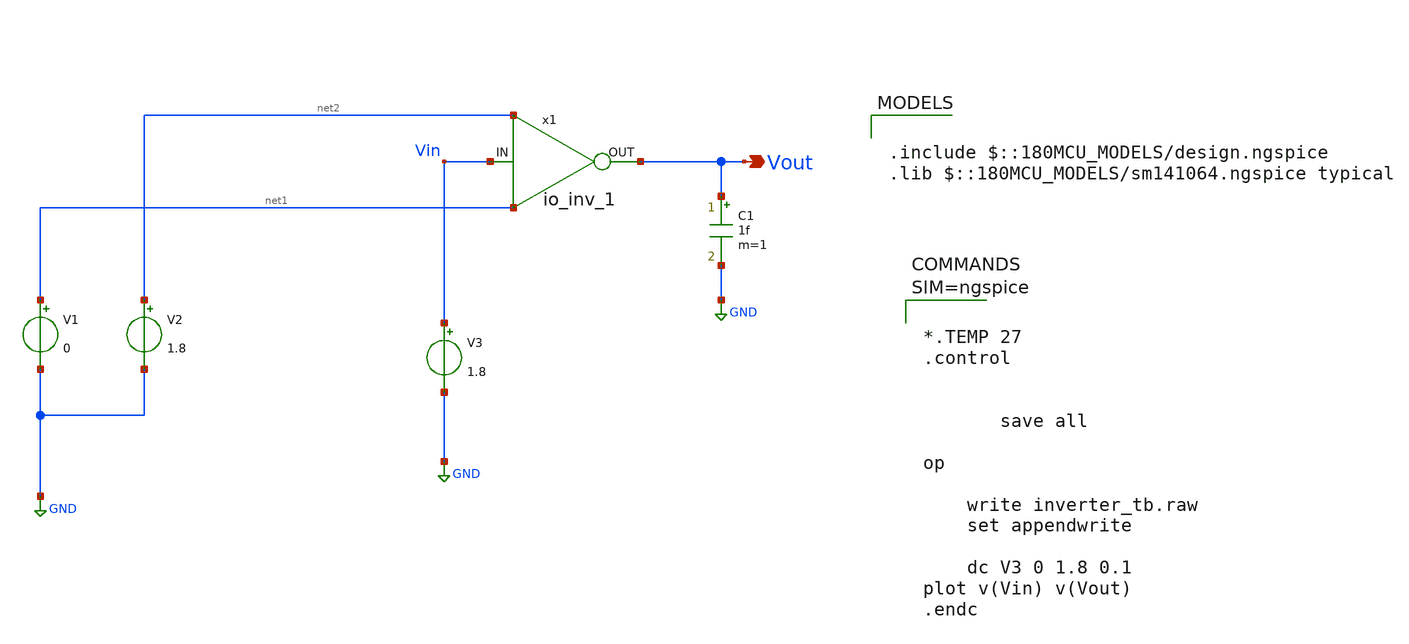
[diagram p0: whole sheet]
** sch_path: xschem/io_inv_1_dc.sch
* Copyright 2023 David Mitchell Bailey
* Licensed under the Apache License, Version 2.0 (the "License");
* you may not use this file except in compliance with the License.
* You may obtain a copy of the License at
* https://www.apache.org/licenses/LICENSE-2.0
* Unless required by applicable law or agreed to in writing, software
* distributed under the License is distributed on an "AS IS" BASIS,
* WITHOUT WARRANTIES OR CONDITIONS OF ANY KIND, either express or implied.
* See the License for the specific language governing permissions and
* limitations under the License.
**.subckt io_inv_1_dc Vout
*.opin Vout
x1 Vin Vout net2 net1 io_inv_1
V1 net1 GND 0
V2 net2 GND 1.8
V3 Vin GND 1.8
C1 Vout GND 1f m=1
**** begin user architecture code

.include $::180MCU_MODELS/design.ngspice
.lib $::180MCU_MODELS/sm141064.ngspice typical




*.TEMP 27
.control


	   save all

op

    write inverter_tb.raw
    set appendwrite

	dc V3 0 1.8 0.1
plot v(Vin) v(Vout)
.endc




**** end user architecture code
**.ends
.GLOBAL GND
.end
